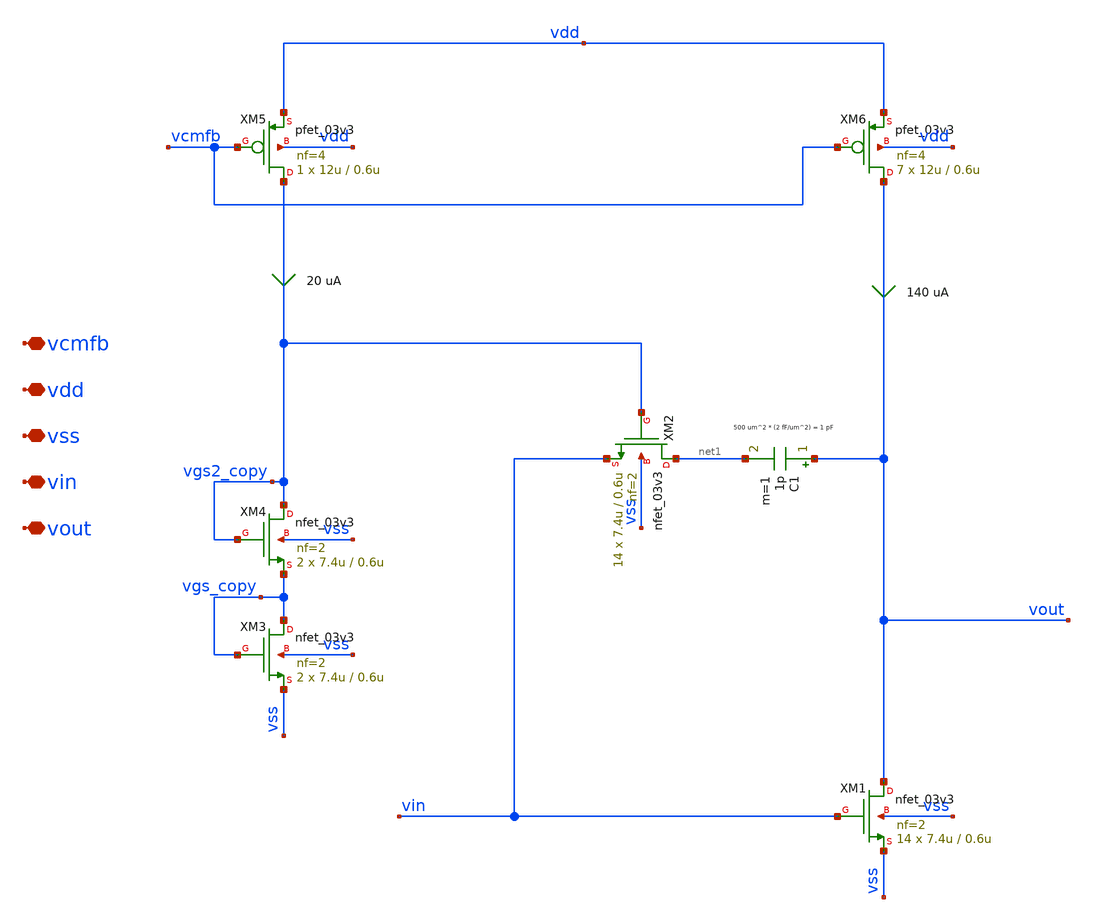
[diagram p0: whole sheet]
** sch_path: xschem/ota/s2_half_circuit.sch
**.subckt s2_half_circuit vcmfb vdd vss vin vout
*.iopin vcmfb
*.iopin vdd
*.iopin vss
*.iopin vin
*.iopin vout
XM6 vout vcmfb vdd vdd pfet_03v3 L=0.6u W=12u nf=4 ad='int((nf+1)/2) * W/nf * 0.18u' as='int((nf+2)/2) * W/nf * 0.18u'
+ pd='2*int((nf+1)/2) * (W/nf + 0.18u)' ps='2*int((nf+2)/2) * (W/nf + 0.18u)' nrd='0.18u / W' nrs='0.18u / W'
+ sa=0 sb=0 sd=0 m=7
XM5 vgs2_copy vcmfb vdd vdd pfet_03v3 L=0.6u W=12u nf=4 ad='int((nf+1)/2) * W/nf * 0.18u' as='int((nf+2)/2) * W/nf * 0.18u'
+ pd='2*int((nf+1)/2) * (W/nf + 0.18u)' ps='2*int((nf+2)/2) * (W/nf + 0.18u)' nrd='0.18u / W' nrs='0.18u / W'
+ sa=0 sb=0 sd=0 m=1
XM1 vout vin vss vss nfet_03v3 L=0.6u W=7.4u nf=2 ad='int((nf+1)/2) * W/nf * 0.18u' as='int((nf+2)/2) * W/nf * 0.18u'
+ pd='2*int((nf+1)/2) * (W/nf + 0.18u)' ps='2*int((nf+2)/2) * (W/nf + 0.18u)' nrd='0.18u / W' nrs='0.18u / W'
+ sa=0 sb=0 sd=0 m=14
XM3 vgs_copy vgs_copy vss vss nfet_03v3 L=0.6u W=7.4u nf=2 ad='int((nf+1)/2) * W/nf * 0.18u' as='int((nf+2)/2) * W/nf * 0.18u'
+ pd='2*int((nf+1)/2) * (W/nf + 0.18u)' ps='2*int((nf+2)/2) * (W/nf + 0.18u)' nrd='0.18u / W' nrs='0.18u / W'
+ sa=0 sb=0 sd=0 m=2
XM4 vgs2_copy vgs2_copy vgs_copy vss nfet_03v3 L=0.6u W=7.4u nf=2 ad='int((nf+1)/2) * W/nf * 0.18u' as='int((nf+2)/2) * W/nf * 0.18u'
+ pd='2*int((nf+1)/2) * (W/nf + 0.18u)' ps='2*int((nf+2)/2) * (W/nf + 0.18u)' nrd='0.18u / W' nrs='0.18u / W'
+ sa=0 sb=0 sd=0 m=2
XM2 net1 vgs2_copy vin vss nfet_03v3 L=0.6u W=7.4u nf=2 ad='int((nf+1)/2) * W/nf * 0.18u' as='int((nf+2)/2) * W/nf * 0.18u'
+ pd='2*int((nf+1)/2) * (W/nf + 0.18u)' ps='2*int((nf+2)/2) * (W/nf + 0.18u)' nrd='0.18u / W' nrs='0.18u / W'
+ sa=0 sb=0 sd=0 m=14
C1 vout net1 1p m=1
**.ends
.end
